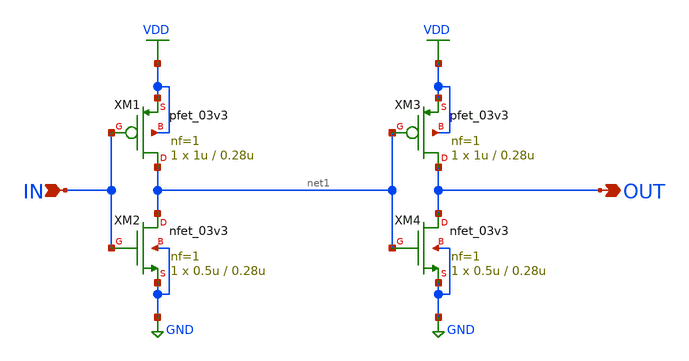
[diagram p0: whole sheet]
** sch_path: BUF.sch
**.subckt BUF IN OUT
*.ipin IN
*.opin OUT
XM1 net1 IN VDD VDD pfet_03v3 L=0.28u W=1u nf=1 ad='int((nf+1)/2) * W/nf * 0.18u' as='int((nf+2)/2) * W/nf * 0.18u'
+ pd='2*int((nf+1)/2) * (W/nf + 0.18u)' ps='2*int((nf+2)/2) * (W/nf + 0.18u)' nrd='0.18u / W' nrs='0.18u / W'
+ sa=0 sb=0 sd=0 m=1
XM2 net1 IN GND GND nfet_03v3 L=0.28u W=0.5u nf=1 ad='int((nf+1)/2) * W/nf * 0.18u' as='int((nf+2)/2) * W/nf * 0.18u'
+ pd='2*int((nf+1)/2) * (W/nf + 0.18u)' ps='2*int((nf+2)/2) * (W/nf + 0.18u)' nrd='0.18u / W' nrs='0.18u / W'
+ sa=0 sb=0 sd=0 m=1
XM3 OUT net1 VDD VDD pfet_03v3 L=0.28u W=1u nf=1 ad='int((nf+1)/2) * W/nf * 0.18u' as='int((nf+2)/2) * W/nf * 0.18u'
+ pd='2*int((nf+1)/2) * (W/nf + 0.18u)' ps='2*int((nf+2)/2) * (W/nf + 0.18u)' nrd='0.18u / W' nrs='0.18u / W'
+ sa=0 sb=0 sd=0 m=1
XM4 OUT net1 GND GND nfet_03v3 L=0.28u W=0.5u nf=1 ad='int((nf+1)/2) * W/nf * 0.18u' as='int((nf+2)/2) * W/nf * 0.18u'
+ pd='2*int((nf+1)/2) * (W/nf + 0.18u)' ps='2*int((nf+2)/2) * (W/nf + 0.18u)' nrd='0.18u / W' nrs='0.18u / W'
+ sa=0 sb=0 sd=0 m=1
**.ends
.GLOBAL VDD
.GLOBAL GND
.end
